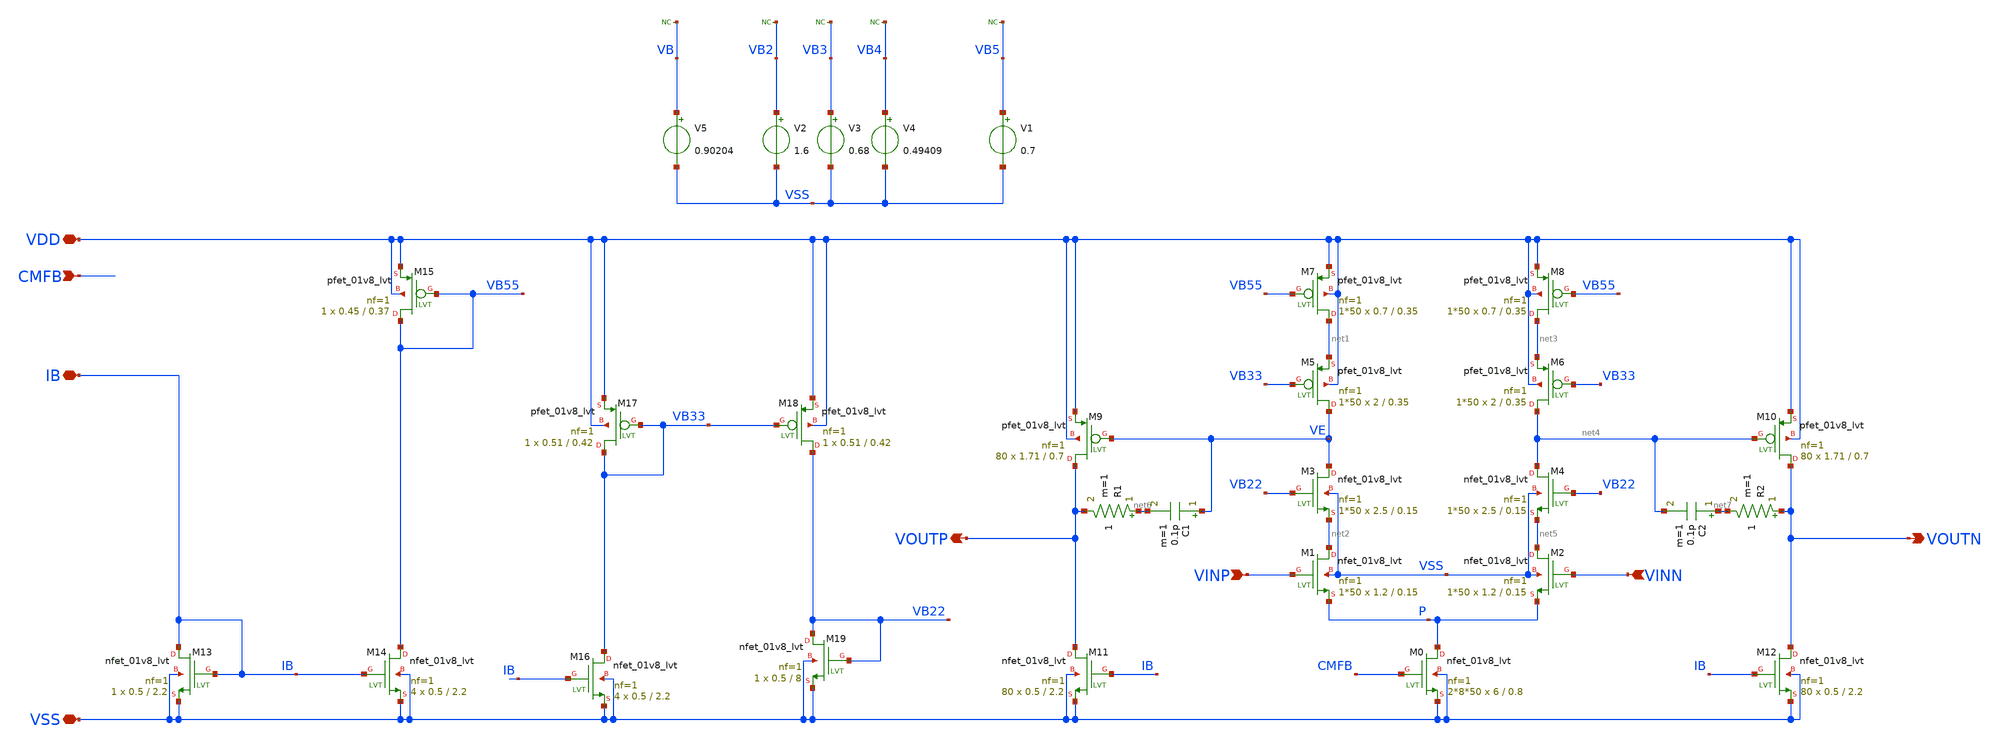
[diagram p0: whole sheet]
** sch_path: Differential_OTA_Telescopic_IHP/OTA_Telescopic_core.sch
**.subckt OTA_Telescopic_core VDD VSS VINP VINN VOUTN VOUTP CMFB IB
*.iopin VDD
*.iopin VSS
*.ipin VINP
*.ipin VINN
*.opin VOUTN
*.opin VOUTP
*.ipin CMFB
*.iopin IB
V2 VB2 VSS 1.6
V3 VB3 VSS 0.68
V4 VB4 VSS 0.49409
XM0 P CMFB VSS VSS sky130_fd_pr__nfet_01v8_lvt L=0.8 W=6 nf=1 ad='int((nf+1)/2) * W/nf * 0.29' as='int((nf+2)/2) * W/nf * 0.29'
+ pd='2*int((nf+1)/2) * (W/nf + 0.29)' ps='2*int((nf+2)/2) * (W/nf + 0.29)' nrd='0.29 / W' nrs='0.29 / W'
+ sa=0 sb=0 sd=0 mult=2*8*50 m=2*8*50
XM1 net2 VINP P VSS sky130_fd_pr__nfet_01v8_lvt L=0.15 W=1.2 nf=1 ad='int((nf+1)/2) * W/nf * 0.29' as='int((nf+2)/2) * W/nf * 0.29'
+ pd='2*int((nf+1)/2) * (W/nf + 0.29)' ps='2*int((nf+2)/2) * (W/nf + 0.29)' nrd='0.29 / W' nrs='0.29 / W'
+ sa=0 sb=0 sd=0 mult=1*50 m=1*50
XM2 net5 VINN P VSS sky130_fd_pr__nfet_01v8_lvt L=0.15 W=1.2 nf=1 ad='int((nf+1)/2) * W/nf * 0.29' as='int((nf+2)/2) * W/nf * 0.29'
+ pd='2*int((nf+1)/2) * (W/nf + 0.29)' ps='2*int((nf+2)/2) * (W/nf + 0.29)' nrd='0.29 / W' nrs='0.29 / W'
+ sa=0 sb=0 sd=0 mult=1*50 m=1*50
XM3 VE VB22 net2 VSS sky130_fd_pr__nfet_01v8_lvt L=0.15 W=2.5 nf=1 ad='int((nf+1)/2) * W/nf * 0.29' as='int((nf+2)/2) * W/nf * 0.29'
+ pd='2*int((nf+1)/2) * (W/nf + 0.29)' ps='2*int((nf+2)/2) * (W/nf + 0.29)' nrd='0.29 / W' nrs='0.29 / W'
+ sa=0 sb=0 sd=0 mult=1*50 m=1*50
XM4 net4 VB22 net5 VSS sky130_fd_pr__nfet_01v8_lvt L=0.15 W=2.5 nf=1 ad='int((nf+1)/2) * W/nf * 0.29'
+ as='int((nf+2)/2) * W/nf * 0.29' pd='2*int((nf+1)/2) * (W/nf + 0.29)' ps='2*int((nf+2)/2) * (W/nf + 0.29)'
+ nrd='0.29 / W' nrs='0.29 / W' sa=0 sb=0 sd=0 mult=1*50 m=1*50
XM5 VE VB33 net1 VDD sky130_fd_pr__pfet_01v8_lvt L=0.35 W=2 nf=1 ad='int((nf+1)/2) * W/nf * 0.29' as='int((nf+2)/2) * W/nf * 0.29'
+ pd='2*int((nf+1)/2) * (W/nf + 0.29)' ps='2*int((nf+2)/2) * (W/nf + 0.29)' nrd='0.29 / W' nrs='0.29 / W'
+ sa=0 sb=0 sd=0 mult=1*50 m=1*50
XM6 net4 VB33 net3 VDD sky130_fd_pr__pfet_01v8_lvt L=0.35 W=2 nf=1 ad='int((nf+1)/2) * W/nf * 0.29' as='int((nf+2)/2) * W/nf * 0.29'
+ pd='2*int((nf+1)/2) * (W/nf + 0.29)' ps='2*int((nf+2)/2) * (W/nf + 0.29)' nrd='0.29 / W' nrs='0.29 / W'
+ sa=0 sb=0 sd=0 mult=1*50 m=1*50
XM7 net1 VB55 VDD VDD sky130_fd_pr__pfet_01v8_lvt L=0.35 W=0.7 nf=1 ad='int((nf+1)/2) * W/nf * 0.29'
+ as='int((nf+2)/2) * W/nf * 0.29' pd='2*int((nf+1)/2) * (W/nf + 0.29)' ps='2*int((nf+2)/2) * (W/nf + 0.29)'
+ nrd='0.29 / W' nrs='0.29 / W' sa=0 sb=0 sd=0 mult=1*50 m=1*50
XM8 net3 VB55 VDD VDD sky130_fd_pr__pfet_01v8_lvt L=0.35 W=0.7 nf=1 ad='int((nf+1)/2) * W/nf * 0.29'
+ as='int((nf+2)/2) * W/nf * 0.29' pd='2*int((nf+1)/2) * (W/nf + 0.29)' ps='2*int((nf+2)/2) * (W/nf + 0.29)'
+ nrd='0.29 / W' nrs='0.29 / W' sa=0 sb=0 sd=0 mult=1*50 m=1*50
XM9 VOUTP VE VDD VDD sky130_fd_pr__pfet_01v8_lvt L=0.7 W=1.71 nf=1 ad='int((nf+1)/2) * W/nf * 0.29' as='int((nf+2)/2) * W/nf * 0.29'
+ pd='2*int((nf+1)/2) * (W/nf + 0.29)' ps='2*int((nf+2)/2) * (W/nf + 0.29)' nrd='0.29 / W' nrs='0.29 / W'
+ sa=0 sb=0 sd=0 mult=80 m=80
XM12 VOUTN IB VSS VSS sky130_fd_pr__nfet_01v8_lvt L=2.2 W=0.5 nf=1 ad='int((nf+1)/2) * W/nf * 0.29' as='int((nf+2)/2) * W/nf * 0.29'
+ pd='2*int((nf+1)/2) * (W/nf + 0.29)' ps='2*int((nf+2)/2) * (W/nf + 0.29)' nrd='0.29 / W' nrs='0.29 / W'
+ sa=0 sb=0 sd=0 mult=80 m=80
XM11 VOUTP IB VSS VSS sky130_fd_pr__nfet_01v8_lvt L=2.2 W=0.5 nf=1 ad='int((nf+1)/2) * W/nf * 0.29' as='int((nf+2)/2) * W/nf * 0.29'
+ pd='2*int((nf+1)/2) * (W/nf + 0.29)' ps='2*int((nf+2)/2) * (W/nf + 0.29)' nrd='0.29 / W' nrs='0.29 / W'
+ sa=0 sb=0 sd=0 mult=80 m=80
XM10 VOUTN net4 VDD VDD sky130_fd_pr__pfet_01v8_lvt L=0.7 W=1.71 nf=1 ad='int((nf+1)/2) * W/nf * 0.29'
+ as='int((nf+2)/2) * W/nf * 0.29' pd='2*int((nf+1)/2) * (W/nf + 0.29)' ps='2*int((nf+2)/2) * (W/nf + 0.29)'
+ nrd='0.29 / W' nrs='0.29 / W' sa=0 sb=0 sd=0 mult=80 m=80
XM13 IB IB VSS VSS sky130_fd_pr__nfet_01v8_lvt L=2.2 W=0.5 nf=1 ad='int((nf+1)/2) * W/nf * 0.29' as='int((nf+2)/2) * W/nf * 0.29'
+ pd='2*int((nf+1)/2) * (W/nf + 0.29)' ps='2*int((nf+2)/2) * (W/nf + 0.29)' nrd='0.29 / W' nrs='0.29 / W'
+ sa=0 sb=0 sd=0 mult=1 m=1
V1 VB5 VSS 0.7
XM14 VB55 IB VSS VSS sky130_fd_pr__nfet_01v8_lvt L=2.2 W=0.5 nf=1 ad='int((nf+1)/2) * W/nf * 0.29' as='int((nf+2)/2) * W/nf * 0.29'
+ pd='2*int((nf+1)/2) * (W/nf + 0.29)' ps='2*int((nf+2)/2) * (W/nf + 0.29)' nrd='0.29 / W' nrs='0.29 / W'
+ sa=0 sb=0 sd=0 mult=4 m=4
XM15 VB55 VB55 VDD VDD sky130_fd_pr__pfet_01v8_lvt L=0.37 W=0.45 nf=1 ad='int((nf+1)/2) * W/nf * 0.29'
+ as='int((nf+2)/2) * W/nf * 0.29' pd='2*int((nf+1)/2) * (W/nf + 0.29)' ps='2*int((nf+2)/2) * (W/nf + 0.29)'
+ nrd='0.29 / W' nrs='0.29 / W' sa=0 sb=0 sd=0 mult=1 m=1
XM16 VB33 IB VSS VSS sky130_fd_pr__nfet_01v8_lvt L=2.2 W=0.5 nf=1 ad='int((nf+1)/2) * W/nf * 0.29' as='int((nf+2)/2) * W/nf * 0.29'
+ pd='2*int((nf+1)/2) * (W/nf + 0.29)' ps='2*int((nf+2)/2) * (W/nf + 0.29)' nrd='0.29 / W' nrs='0.29 / W'
+ sa=0 sb=0 sd=0 mult=4 m=4
XM17 VB33 VB33 VDD VDD sky130_fd_pr__pfet_01v8_lvt L=0.42 W=0.51 nf=1 ad='int((nf+1)/2) * W/nf * 0.29'
+ as='int((nf+2)/2) * W/nf * 0.29' pd='2*int((nf+1)/2) * (W/nf + 0.29)' ps='2*int((nf+2)/2) * (W/nf + 0.29)'
+ nrd='0.29 / W' nrs='0.29 / W' sa=0 sb=0 sd=0 mult=1 m=1
XM18 VB22 VB33 VDD VDD sky130_fd_pr__pfet_01v8_lvt L=0.42 W=0.51 nf=1 ad='int((nf+1)/2) * W/nf * 0.29'
+ as='int((nf+2)/2) * W/nf * 0.29' pd='2*int((nf+1)/2) * (W/nf + 0.29)' ps='2*int((nf+2)/2) * (W/nf + 0.29)'
+ nrd='0.29 / W' nrs='0.29 / W' sa=0 sb=0 sd=0 mult=1 m=1
XM19 VB22 VB22 VSS VSS sky130_fd_pr__nfet_01v8_lvt L=8 W=0.5 nf=1 ad='int((nf+1)/2) * W/nf * 0.29' as='int((nf+2)/2) * W/nf * 0.29'
+ pd='2*int((nf+1)/2) * (W/nf + 0.29)' ps='2*int((nf+2)/2) * (W/nf + 0.29)' nrd='0.29 / W' nrs='0.29 / W'
+ sa=0 sb=0 sd=0 mult=1 m=1
* noconn VB2
* noconn VB3
* noconn VB4
* noconn VB5
V5 VB VSS 0.90204
* noconn VB
R1 net6 VOUTP 1 m=1
R2 VOUTN net7 1 m=1
C1 VE net6 0.1p m=1
C2 net7 net4 0.1p m=1
**.ends
.end
